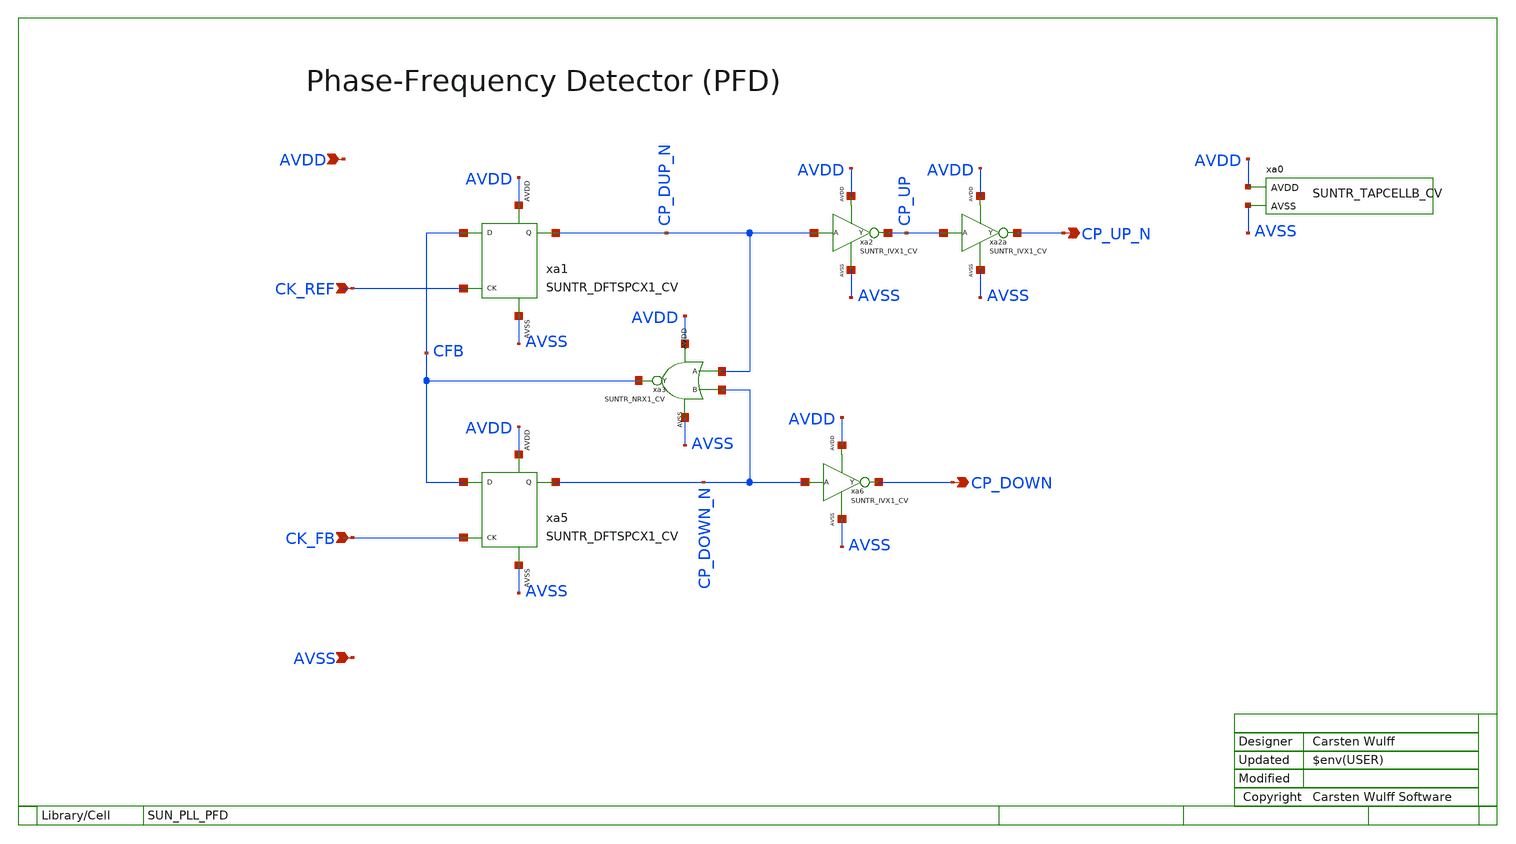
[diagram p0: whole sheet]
** sch_path: ip/sun_pll_sky130nm/design/SUN_PLL_SKY130NM/SUN_PLL_PFD.sch
**.subckt SUN_PLL_PFD CK_FB CK_REF CP_UP_N CP_DOWN AVDD AVSS
*.ipin CK_FB
*.ipin CK_REF
*.opin CP_UP_N
*.opin CP_DOWN
*.ipin AVDD
*.ipin AVSS
xa3 CP_DUP_N CP_DOWN_N CFB AVDD AVSS SUNTR_NRX1_CV xoffset=0 yoffset=0 angle=0 M=1
xa2 CP_DUP_N CP_UP AVDD AVSS SUNTR_IVX1_CV
xa6 CP_DOWN_N CP_DOWN AVDD AVSS SUNTR_IVX1_CV
xa1 CFB CK_REF CP_DUP_N AVDD AVSS SUNTR_DFTSPCX1_CV xoffset=0 yoffset=0 angle=0 M=1
xa5 CFB CK_FB CP_DOWN_N AVDD AVSS SUNTR_DFTSPCX1_CV xoffset=0 yoffset=0 angle=0 M=1
xa0 AVDD AVSS SUNTR_TAPCELLB_CV
xa2a CP_UP CP_UP_N AVDD AVSS SUNTR_IVX1_CV
**.ends
.end
